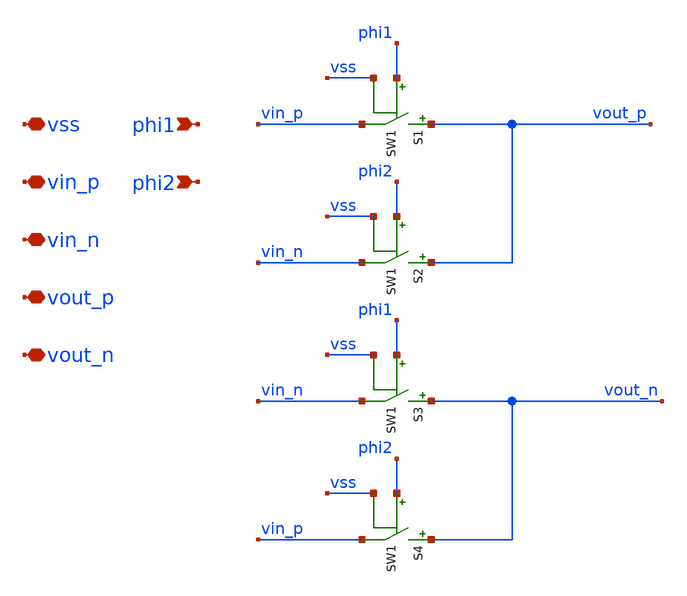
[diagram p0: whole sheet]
** sch_path: xschem/archive/chopper_bhv/chopper_ideal.sch
**.subckt chopper_ideal vss vin_p vin_n vout_p vout_n phi1 phi2
*.iopin vss
*.iopin vin_p
*.iopin vin_n
*.iopin vout_p
*.iopin vout_n
*.ipin phi1
*.ipin phi2
S1 vout_p vin_p phi1 vss SW1
S2 vout_p vin_n phi2 vss SW1
S3 vout_n vin_n phi1 vss SW1
S4 vout_n vin_p phi2 vss SW1
**.ends
**** begin user architecture code
.MODEL SW1 SW   VT=1.65 VH=0  RON=0.01 ROFF=10G
**** end user architecture code
.end
